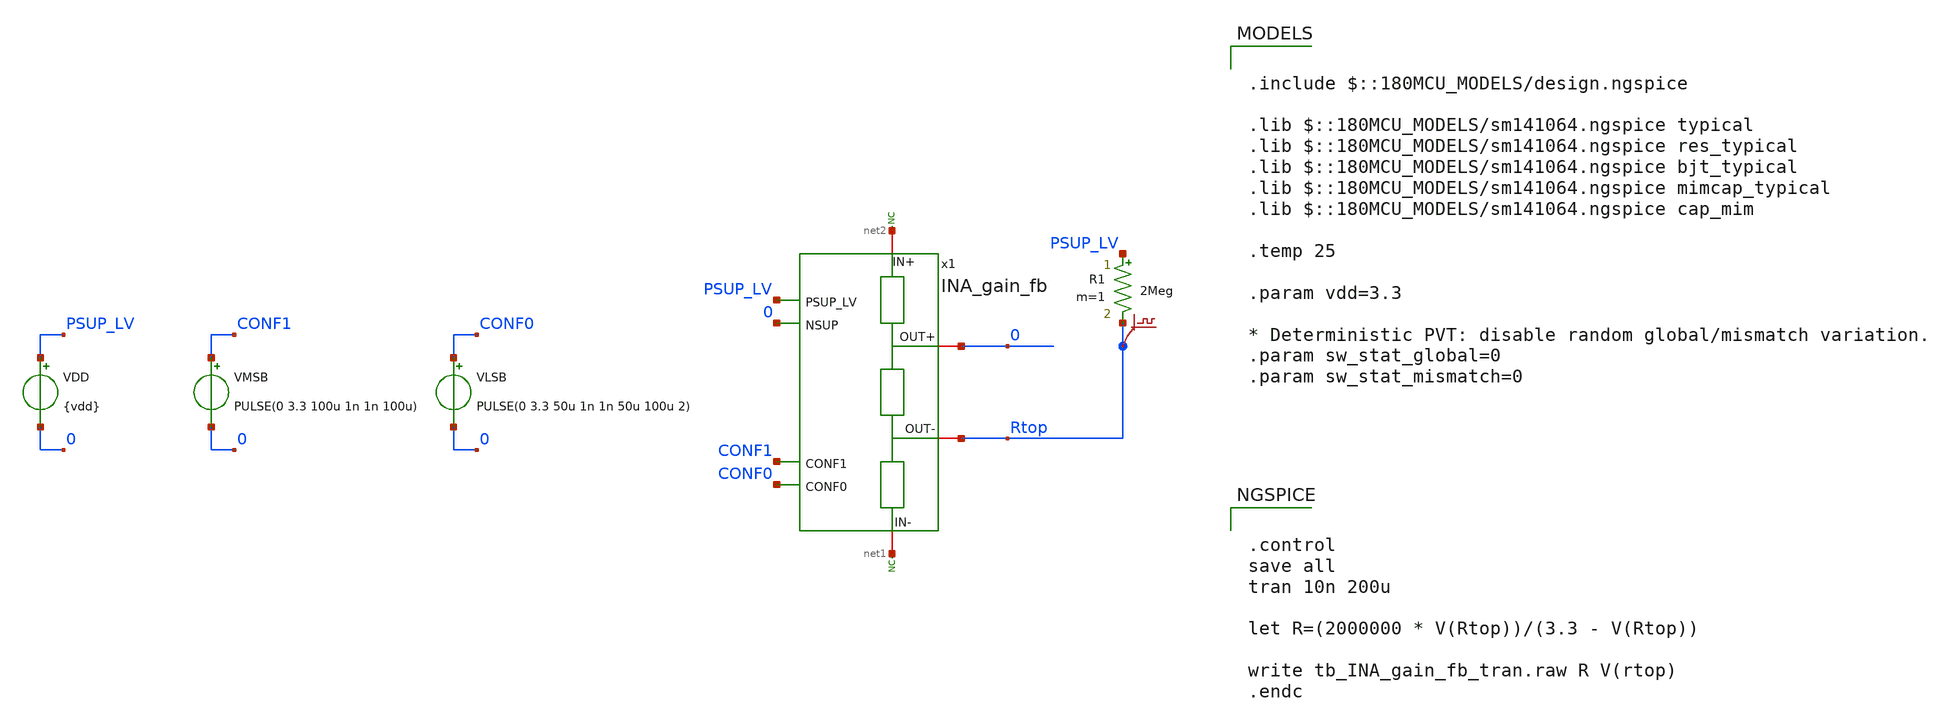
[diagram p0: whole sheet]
** sch_path: xschem/blocks/INA_gain_fb/tb_INA_gain_fb_tran.sch
**.subckt tb_INA_gain_fb_tran
VLSB CONF0 0 PULSE(0 3.3 50u 1n 1n 50u 100u 2)
VMSB CONF1 0 PULSE(0 3.3 100u 1n 1n 100u)
VDD PSUP_LV 0 {vdd}
* noconn #net1
* noconn #net2
R1 PSUP_LV Rtop 2Meg m=1
.save v(rtop)
x1 net2 0 PSUP_LV 0 CONF1 CONF0 Rtop net1 INA_gain_fb
**** begin user architecture code

.include $::180MCU_MODELS/design.ngspice

.lib $::180MCU_MODELS/sm141064.ngspice typical
.lib $::180MCU_MODELS/sm141064.ngspice res_typical
.lib $::180MCU_MODELS/sm141064.ngspice bjt_typical
.lib $::180MCU_MODELS/sm141064.ngspice mimcap_typical
.lib $::180MCU_MODELS/sm141064.ngspice cap_mim

.temp 25

.param vdd=3.3

* Deterministic PVT: disable random global/mismatch variation.
.param sw_stat_global=0
.param sw_stat_mismatch=0



.control
save all
tran 10n 200u

let R=(2000000 * V(Rtop))/(3.3 - V(Rtop))

write tb_INA_gain_fb_tran.raw R V(rtop)
.endc


**** end user architecture code
**.ends

* expanding   symbol:  blocks/INA_gain_fb/INA_gain_fb.sym # of pins=8
** sym_path: xschem/blocks/INA_gain_fb/INA_gain_fb.sym
** sch_path: xschem/blocks/INA_gain_fb/INA_gain_fb.sch
.subckt INA_gain_fb IN+ OUT+ PSUP_LV NSUP CONF1 CONF0 OUT- IN-
*.iopin IN+
*.iopin IN-
*.iopin OUT-
*.iopin OUT+
*.ipin PSUP_LV
*.ipin NSUP
*.ipin CONF0
*.ipin CONF1
XR6 net8 net2 PSUP_LV ppolyf_u_3k r_width=1e-6 r_length=0.6e-6 m=1
* noconn NSUP
* noconn PSUP_LV
x3 PSUP_LV CONF0 nCONF0 NSUP not
x4 PSUP_LV CONF1 nCONF1 NSUP not
x5 nC3 CONF1 CONF0 PSUP_LV NSUP nand_2
x6 nC2 CONF1 nCONF0 PSUP_LV NSUP nand_2
x8 nC1 nCONF1 CONF0 PSUP_LV NSUP nand_2
* noconn NSUP
* noconn PSUP_LV
x9 PSUP_LV nC3 C3 NSUP not
x10 PSUP_LV nC2 C2 NSUP not
x11 PSUP_LV nC1 C1 NSUP not
* noconn NSUP
* noconn PSUP_LV
XR10 IN- net1 PSUP_LV ppolyf_u_1k r_width=1e-6 r_length=1e-3 m=1
XR3 net1 net6 PSUP_LV ppolyf_u_1k r_width=1e-6 r_length=900e-6 m=1
XR8 net6 net7 PSUP_LV ppolyf_u_1k r_width=1e-6 r_length=90e-6 m=1
XR7 net7 net8 PSUP_LV ppolyf_u_1k r_width=1e-6 r_length=9e-6 m=1
XR2 net2 net3 PSUP_LV ppolyf_u_1k r_width=1e-6 r_length=9e-6 m=1
XR4 net3 net4 PSUP_LV ppolyf_u_1k r_width=1e-6 r_length=90e-6 m=1
XR5 net4 net5 PSUP_LV ppolyf_u_1k r_width=1e-6 r_length=900e-6 m=1
XR1 net5 IN+ PSUP_LV ppolyf_u_1k r_width=1e-6 r_length=1e-3 m=1
x1 net9 net10 net11 net12 net13 net14 transmission_gate
x2 net15 net16 net17 net18 net19 net20 transmission_gate
x7 net21 net22 net23 net24 net25 net26 transmission_gate
x12 net27 net28 net29 net30 net31 net32 transmission_gate
x13 nC0 nCONF1 nCONF0 PSUP_LV NSUP nand_2
x14 PSUP_LV nC0 C0 NSUP not
.ends


* expanding   symbol:  blocks/not/not.sym # of pins=6
** sym_path: xschem/blocks/not/not.sym
** sch_path: xschem/blocks/not/not.sch
.subckt not PSUP A B NSUP
*.ipin PSUP
*.ipin NSUP
*.ipin A
*.opin B
XM2 B A NSUP NSUP nfet_03v3 L=0.28u W=0.22u nf=1 ad='int((nf+1)/2) * W/nf * 0.18u' as='int((nf+2)/2) * W/nf * 0.18u'
+ pd='2*int((nf+1)/2) * (W/nf + 0.18u)' ps='2*int((nf+2)/2) * (W/nf + 0.18u)' nrd='0.18u / W' nrs='0.18u / W'
+ sa=0 sb=0 sd=0 m=1
XM1 B A PSUP PSUP pfet_03v3 L=0.28u W=0.5u nf=1 ad='int((nf+1)/2) * W/nf * 0.18u' as='int((nf+2)/2) * W/nf * 0.18u'
+ pd='2*int((nf+1)/2) * (W/nf + 0.18u)' ps='2*int((nf+2)/2) * (W/nf + 0.18u)' nrd='0.18u / W' nrs='0.18u / W'
+ sa=0 sb=0 sd=0 m=1
.ends


* expanding   symbol:  blocks/nand_2/nand_2.sym # of pins=7
** sym_path: xschem/blocks/nand_2/nand_2.sym
** sch_path: xschem/blocks/nand_2/nand_2.sch
.subckt nand_2 Y A B PSUP NSUP
*.ipin PSUP
*.ipin NSUP
*.ipin A
*.ipin B
*.opin Y
XM5 net1 B NSUP NSUP nfet_03v3 L=0.28u W=0.22u nf=1 ad='int((nf+1)/2) * W/nf * 0.18u' as='int((nf+2)/2) * W/nf * 0.18u'
+ pd='2*int((nf+1)/2) * (W/nf + 0.18u)' ps='2*int((nf+2)/2) * (W/nf + 0.18u)' nrd='0.18u / W' nrs='0.18u / W'
+ sa=0 sb=0 sd=0 m=1
XM1 Y A net1 NSUP nfet_03v3 L=0.28u W=0.22u nf=1 ad='int((nf+1)/2) * W/nf * 0.18u' as='int((nf+2)/2) * W/nf * 0.18u'
+ pd='2*int((nf+1)/2) * (W/nf + 0.18u)' ps='2*int((nf+2)/2) * (W/nf + 0.18u)' nrd='0.18u / W' nrs='0.18u / W'
+ sa=0 sb=0 sd=0 m=1
XM2 Y A PSUP PSUP pfet_03v3 L=0.28u W=0.5u nf=1 ad='int((nf+1)/2) * W/nf * 0.18u' as='int((nf+2)/2) * W/nf * 0.18u'
+ pd='2*int((nf+1)/2) * (W/nf + 0.18u)' ps='2*int((nf+2)/2) * (W/nf + 0.18u)' nrd='0.18u / W' nrs='0.18u / W'
+ sa=0 sb=0 sd=0 m=1
XM3 Y B PSUP PSUP pfet_03v3 L=0.28u W=0.5u nf=1 ad='int((nf+1)/2) * W/nf * 0.18u' as='int((nf+2)/2) * W/nf * 0.18u'
+ pd='2*int((nf+1)/2) * (W/nf + 0.18u)' ps='2*int((nf+2)/2) * (W/nf + 0.18u)' nrd='0.18u / W' nrs='0.18u / W'
+ sa=0 sb=0 sd=0 m=1
.ends


* expanding   symbol:  blocks/transmission_gate/transmission_gate.sym # of pins=6
** sym_path: xschem/blocks/transmission_gate/transmission_gate.sym
** sch_path: xschem/blocks/transmission_gate/transmission_gate.sch
.subckt transmission_gate C A B nC VPOS VNEG
*.iopin A
*.iopin B
*.ipin C
*.ipin nC
*.ipin VPOS
*.ipin VNEG
XM3 A C B VNEG nfet_03v3 L=2u W=10u nf=1 ad='int((nf+1)/2) * W/nf * 0.18u' as='int((nf+2)/2) * W/nf * 0.18u'
+ pd='2*int((nf+1)/2) * (W/nf + 0.18u)' ps='2*int((nf+2)/2) * (W/nf + 0.18u)' nrd='0.18u / W' nrs='0.18u / W'
+ sa=0 sb=0 sd=0 m=2
XM4 A nC B VPOS pfet_03v3 L=2u W=10u nf=1 ad='int((nf+1)/2) * W/nf * 0.18u' as='int((nf+2)/2) * W/nf * 0.18u'
+ pd='2*int((nf+1)/2) * (W/nf + 0.18u)' ps='2*int((nf+2)/2) * (W/nf + 0.18u)' nrd='0.18u / W' nrs='0.18u / W'
+ sa=0 sb=0 sd=0 m=4
.ends

.end
